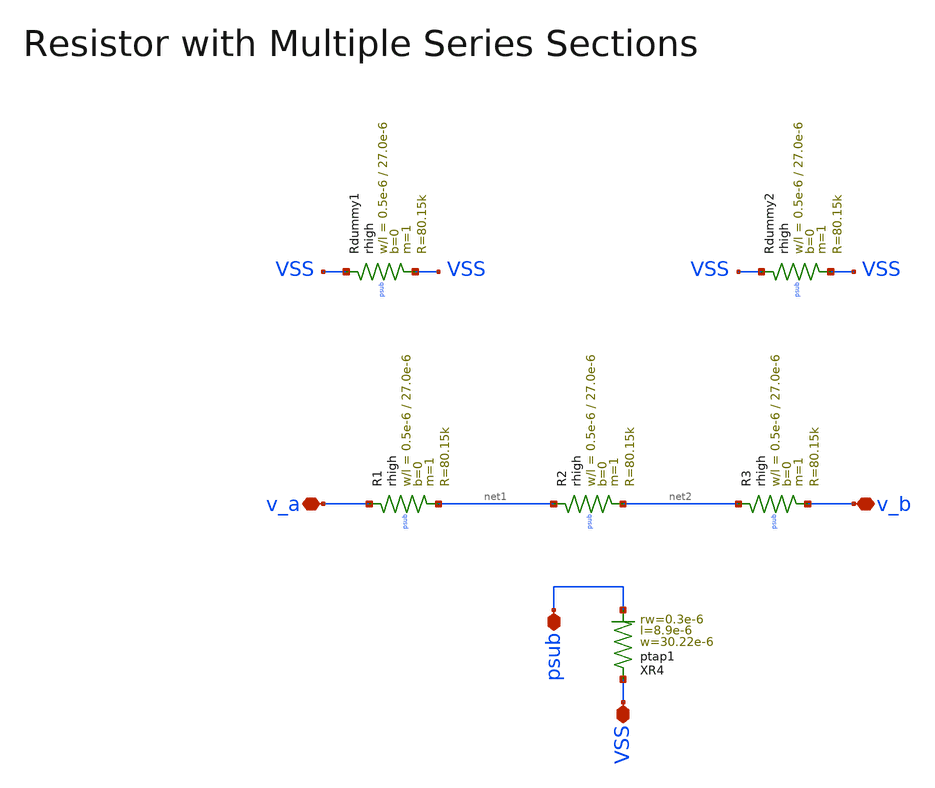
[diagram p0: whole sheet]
** sch_path: ihp130/macros/iqmod/schematic/iqmod_mfb_lpf_R1.sch
**.subckt iqmod_mfb_lpf_R1 v_a v_b VSS psub
*.iopin v_a
*.iopin v_b
*.iopin VSS
*.iopin psub
XR1 v_a net1 psub rhigh w=0.5e-6 l=27.0e-6 m=1 b=0 mm_ok=1
XR2 net1 net2 psub rhigh w=0.5e-6 l=27.0e-6 m=1 b=0 mm_ok=1
XR3 net2 v_b psub rhigh w=0.5e-6 l=27.0e-6 m=1 b=0 mm_ok=1
XRdummy1 VSS VSS psub rhigh w=0.5e-6 l=27.0e-6 m=1 b=0 mm_ok=1
XRdummy2 VSS VSS psub rhigh w=0.5e-6 l=27.0e-6 m=1 b=0 mm_ok=1
XR4 VSS psub ptap1 R=2.958 w=30.22e-6 l=8.9e-6 rw=0.3e-6
**.ends
.end
